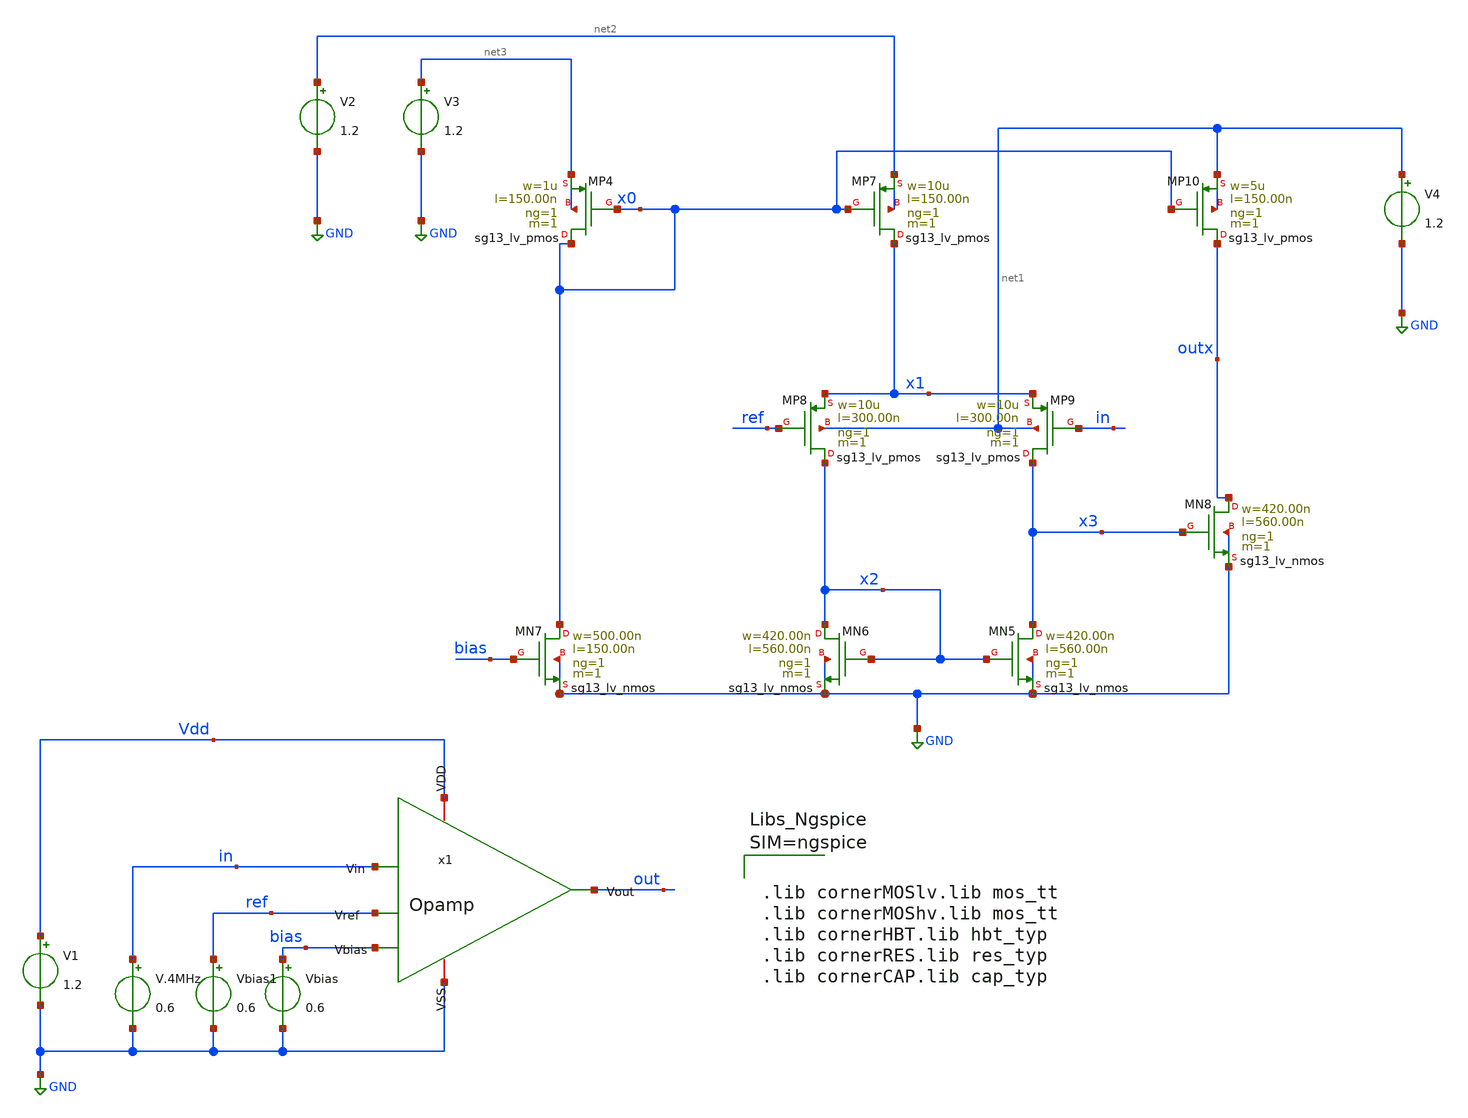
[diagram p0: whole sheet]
** sch_path: schematic/opamptb.sch
**.subckt opamptb
x1 Vdd in ref out bias GND Opamp
V1 Vdd GND 1.2
Vbias1 ref GND 0.6
V.4MHz in GND 0.6
Vbias bias GND 0.6
V2 net2 GND 1.2
V3 net3 GND 1.2
V4 net1 GND 1.2
XMP4 x0 x0 net3 net3 sg13_lv_pmos w=1u l=150.00n ng=1 m=1 mm_ok=1
XMP7 x1 x0 net2 net2 sg13_lv_pmos w=10u l=150.00n ng=1 m=1 mm_ok=1
XMN5 x3 x2 GND GND sg13_lv_nmos w=420.00n l=560.00n ng=1 m=1 mm_ok=1
XMN6 x2 x2 GND GND sg13_lv_nmos w=420.00n l=560.00n ng=1 m=1 mm_ok=1
XMN7 x0 bias GND GND sg13_lv_nmos w=500.00n l=150.00n ng=1 m=1 mm_ok=1
XMP8 x2 ref x1 net1 sg13_lv_pmos w=10u l=300.00n ng=1 m=1 mm_ok=1
XMP9 x3 in x1 net1 sg13_lv_pmos w=10u l=300.00n ng=1 m=1 mm_ok=1
XMN8 outx x3 GND GND sg13_lv_nmos w=420.00n l=560.00n ng=1 m=1 mm_ok=1
XMP10 outx x0 net1 net1 sg13_lv_pmos w=5u l=150.00n ng=1 m=1 mm_ok=1
**** begin user architecture code



.lib cornerMOSlv.lib mos_tt
.lib cornerMOShv.lib mos_tt
.lib cornerHBT.lib hbt_typ
.lib cornerRES.lib res_typ
.lib cornerCAP.lib cap_typ




.tran 1n 1u
.control
run
write /home/designer/shared/opamp.raw
.endc

**** end user architecture code
**.ends

* expanding   symbol:  Opamp.sym # of pins=6
** sym_path: schematic/Opamp.sym
** sch_path: schematic/Opamp.sch
.subckt Opamp VDD Vin Vref Vout Vbias VSS
*.ipin Vin
*.iopin VDD
*.iopin VSS
*.ipin Vref
*.opin Vout
*.ipin Vbias
XMP5 net4 net4 VDD VDD sg13_lv_pmos w=10u l=150.00n ng=1 m=1 mm_ok=1
XMP6 net1 net4 VDD VDD sg13_lv_pmos w=10u l=150.00n ng=1 m=1 mm_ok=1
XMN4 net3 net2 VSS VSS sg13_lv_nmos w=420.00n l=560.00n ng=1 m=1 mm_ok=1
XMN5 net2 net2 VSS VSS sg13_lv_nmos w=420.00n l=560.00n ng=1 m=1 mm_ok=1
XMN6 net4 Vbias VSS VSS sg13_lv_nmos w=500.00n l=150.00n ng=1 m=1 mm_ok=1
XMP7 net2 Vref net1 VDD sg13_lv_pmos w=10u l=300.00n ng=1 m=1 mm_ok=1
XMP8 net3 Vin net1 VDD sg13_lv_pmos w=10u l=300.00n ng=1 m=1 mm_ok=1
XMN7 Vout net3 VSS VSS sg13_lv_nmos w=420.00n l=560.00n ng=1 m=1 mm_ok=1
XMP9 Vout net4 VDD VDD sg13_lv_pmos w=5u l=150.00n ng=1 m=1 mm_ok=1
.ends

.GLOBAL GND
.end
